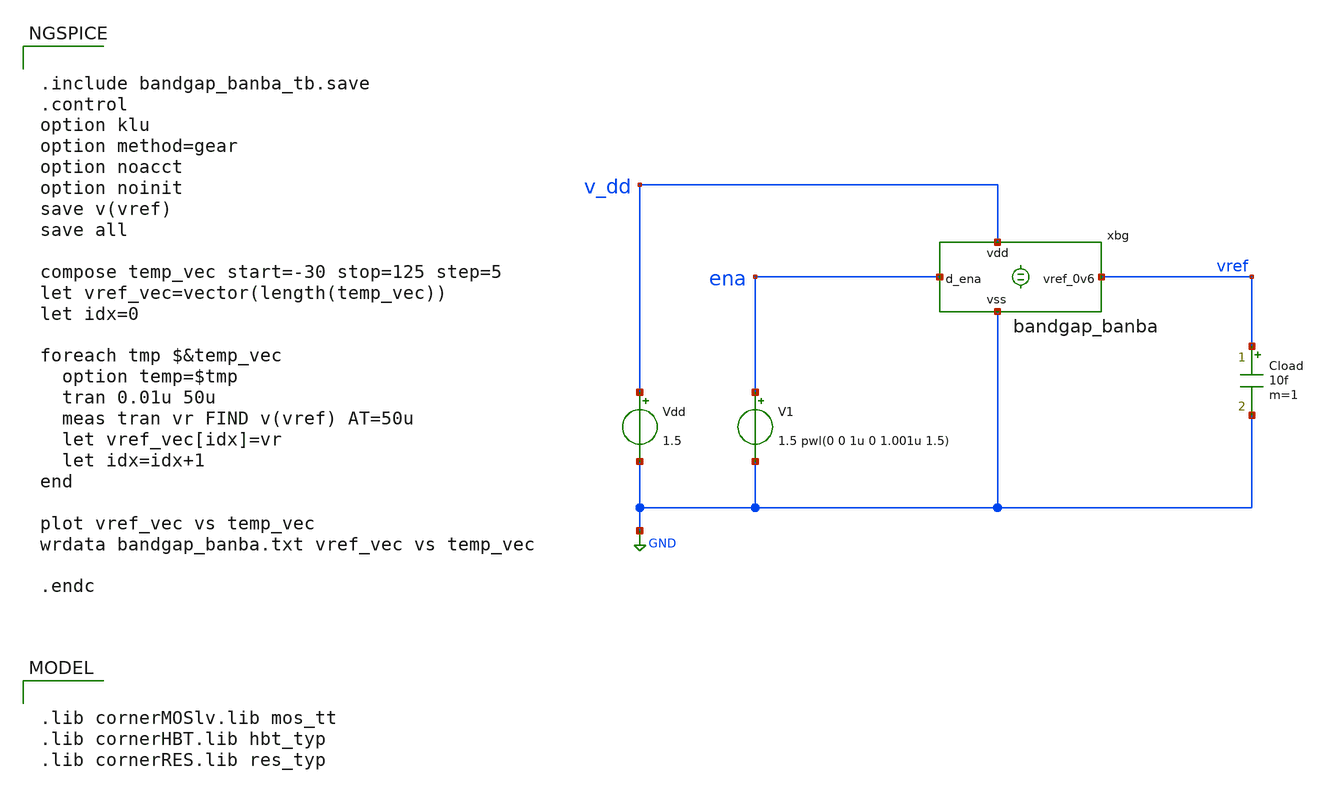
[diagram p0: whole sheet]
** sch_path: xschem/bandgap_banba_tb.sch
* (c) 2025 Harald Pretl, Apache-2.0 license
**.subckt bandgap_banba_tb
Vdd v_dd GND 1.5
.save i(vdd)
V1 ena GND 1.5 pwl(0 0 1u 0 1.001u 1.5)
xbg v_dd ena vref GND bandgap_banba
Cload vref GND 10f m=1
**** begin user architecture code

.lib cornerMOSlv.lib mos_tt
.lib cornerHBT.lib hbt_typ
.lib cornerRES.lib res_typ



.include bandgap_banba_tb.save
.control
option klu
option method=gear
option noacct
option noinit
save v(vref)
save all

compose temp_vec start=-30 stop=125 step=5
let vref_vec=vector(length(temp_vec))
let idx=0

foreach tmp $&temp_vec
  option temp=$tmp
  tran 0.01u 50u
  meas tran vr FIND v(vref) AT=50u
  let vref_vec[idx]=vr
  let idx=idx+1
end

plot vref_vec vs temp_vec
wrdata bandgap_banba.txt vref_vec vs temp_vec

.endc


**** end user architecture code
**.ends
.GLOBAL GND
.end
